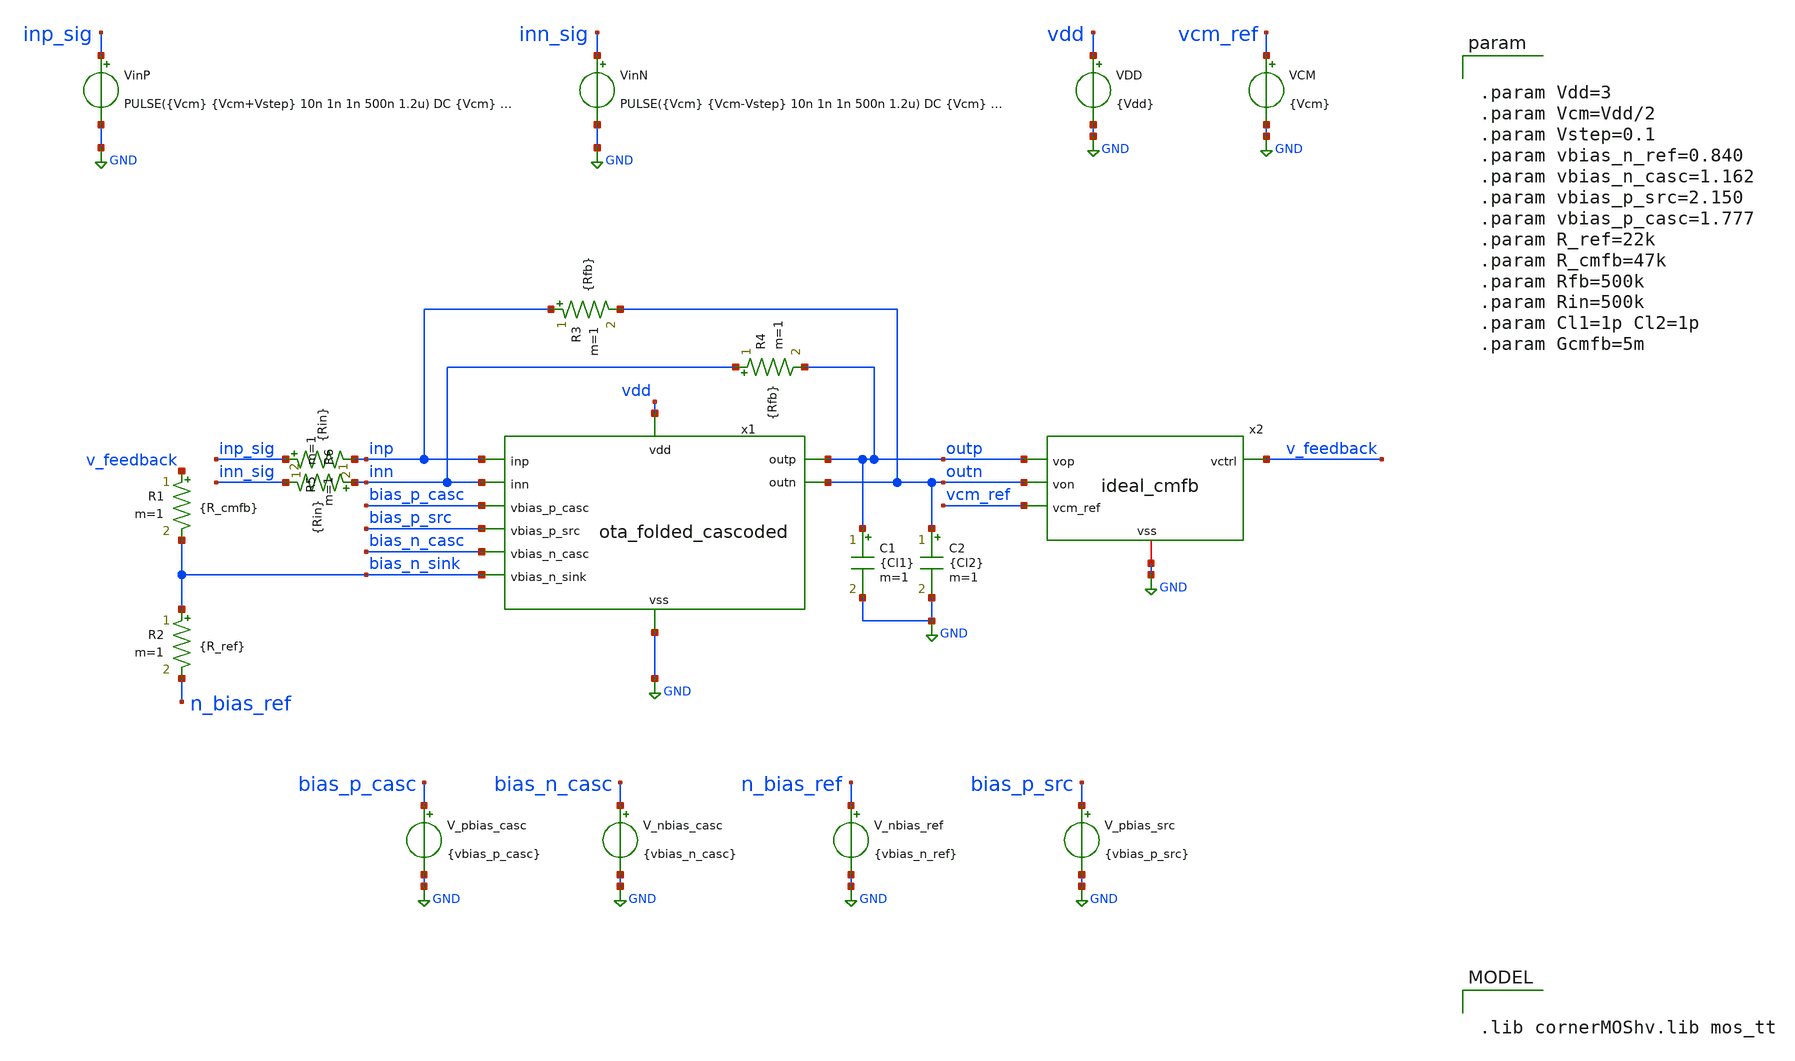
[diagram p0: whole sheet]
** sch_path: 3_real_circuits/ota_ideal_cmfb_unity_buffer.sch
**.subckt ota_ideal_cmfb_unity_buffer
VCM vcm_ref GND {Vcm}
VinP inp_sig GND PULSE({Vcm} {Vcm+Vstep} 10n 1n 1n 500n 1.2u) DC {Vcm} AC 0.5
VinN inn_sig GND PULSE({Vcm} {Vcm-Vstep} 10n 1n 1n 500n 1.2u) DC {Vcm} AC -0.5
x1 inp inn outp GND outn bias_p_casc bias_p_src bias_n_casc bias_n_sink vdd ota_folded_cascoded
VDD vdd GND {Vdd}
x2 outp v_feedback outn vcm_ref GND ideal_cmfb
C2 outn GND {Cl2} m=1
C1 outp GND {Cl1} m=1
V_pbias_casc bias_p_casc GND {vbias_p_casc}
V_nbias_casc bias_n_casc GND {vbias_n_casc}
R1 v_feedback bias_n_sink {R_cmfb} m=1
V_nbias_ref n_bias_ref GND {vbias_n_ref}
V_pbias_src bias_p_src GND {vbias_p_src}
R2 bias_n_sink n_bias_ref {R_ref} m=1
R3 inp outn {Rfb} m=1
R4 inn outp {Rfb} m=1
R5 inp_sig inp {Rin} m=1
R6 inn inn_sig {Rin} m=1
**** begin user architecture code


.option temp=27
.option savecurrents
.control
option sparse
save all
op
write ota_folded_cascoded_tran.raw

tran 100p 1.5u
wrdata ota_tran_small.txt v(outp) v(outn) v(inp) v(inn) v(inp_sig) v(inn_sig)
plot v(outp)-v(outn) title 'Small Signal (100mV)'

alterparam Vstep=0.5
reset

save all
tran 100p 1.5u
wrdata ota_tran_large.txt v(outp) v(outn) v(inp) v(inn) v(inp_sig) v(inn_sig)
plot v(outp)-v(outn) title 'Large Signal (500mV)'

.endc



.lib cornerMOShv.lib mos_tt



.param Vdd=3
.param Vcm=Vdd/2
.param Vstep=0.1
.param vbias_n_ref=0.840
.param vbias_n_casc=1.162
.param vbias_p_src=2.150
.param vbias_p_casc=1.777
.param R_ref=22k
.param R_cmfb=47k
.param Rfb=500k
.param Rin=500k
.param Cl1=1p Cl2=1p
.param Gcmfb=5m


 .include /foss/designs/drms-elie3/3_real_circuits/ota_folded_cascoded_tb.save

**** end user architecture code
**.ends

* expanding   symbol:  ota_folded_cascoded.sym # of pins=12
** sym_path: 3_real_circuits/ota_folded_cascoded.sym
** sch_path: 3_real_circuits/ota_folded_cascoded.sch
.subckt ota_folded_cascoded inp inn outp vss outn vbias_p_casc vbias_p_src vbias_n_casc vbias_n_sink
+ vdd
*.ipin inp
*.ipin inn
*.iopin vss
*.ipin vdd
*.opin outn
*.opin outp
*.ipin vbias_n_casc
*.ipin vbias_p_casc
*.ipin vbias_p_src
*.ipin vbias_n_sink
XM1 net5 inp net1 vss sg13_hv_nmos w=2u l=1u ng=1 m=1 mm_ok=1
XM10 net5 vbias_p_src vdd vdd sg13_hv_pmos w=8.5u l=1u ng=1 m=1 mm_ok=1
XM8 outn vbias_p_casc net5 vdd sg13_hv_pmos w=4u l=1u ng=1 m=1 mm_ok=1
XM11 net4 vbias_p_src vdd vdd sg13_hv_pmos w=8.5u l=1u ng=1 m=1 mm_ok=1
XM9 outp vbias_p_casc net4 vdd sg13_hv_pmos w=4u l=1u ng=1 m=1 mm_ok=1
XM7 outp vbias_n_casc net3 vss sg13_hv_nmos w=1u l=1u ng=1 m=1 mm_ok=1
XM5 net3 vbias_n_sink vss vss sg13_hv_nmos w=1u l=1u ng=1 m=1 mm_ok=1
XM4 net2 vbias_n_sink vss vss sg13_hv_nmos w=1u l=1u ng=1 m=1 mm_ok=1
XM6 outn vbias_n_casc net2 vss sg13_hv_nmos w=1u l=1u ng=1 m=1 mm_ok=1
XM2 net4 inn net1 vss sg13_hv_nmos w=2u l=1u ng=1 m=1 mm_ok=1
XM3 net1 vbias_n_sink vss vss sg13_hv_nmos w=2.5u l=1.0u ng=1 m=1 mm_ok=1
.ends


* expanding   symbol:  ideal_cmfb.sym # of pins=5
** sym_path: 3_real_circuits/ideal_cmfb.sym
** sch_path: 3_real_circuits/ideal_cmfb.sch
.subckt ideal_cmfb vop vctrl von vcm_ref vss
*.opin vctrl
*.ipin vop
*.ipin von
*.ipin vcm_ref
*.iopin vss
B1 voc vss V = (V(vop)+V(von))/2
B2 verr vss V = V(vcm_ref) - V(voc)
B3 vctrl vss I = {Gcmfb}*V(verr)
* noconn vop
* noconn von
* noconn vcm_ref
.ends

.GLOBAL GND
.end
